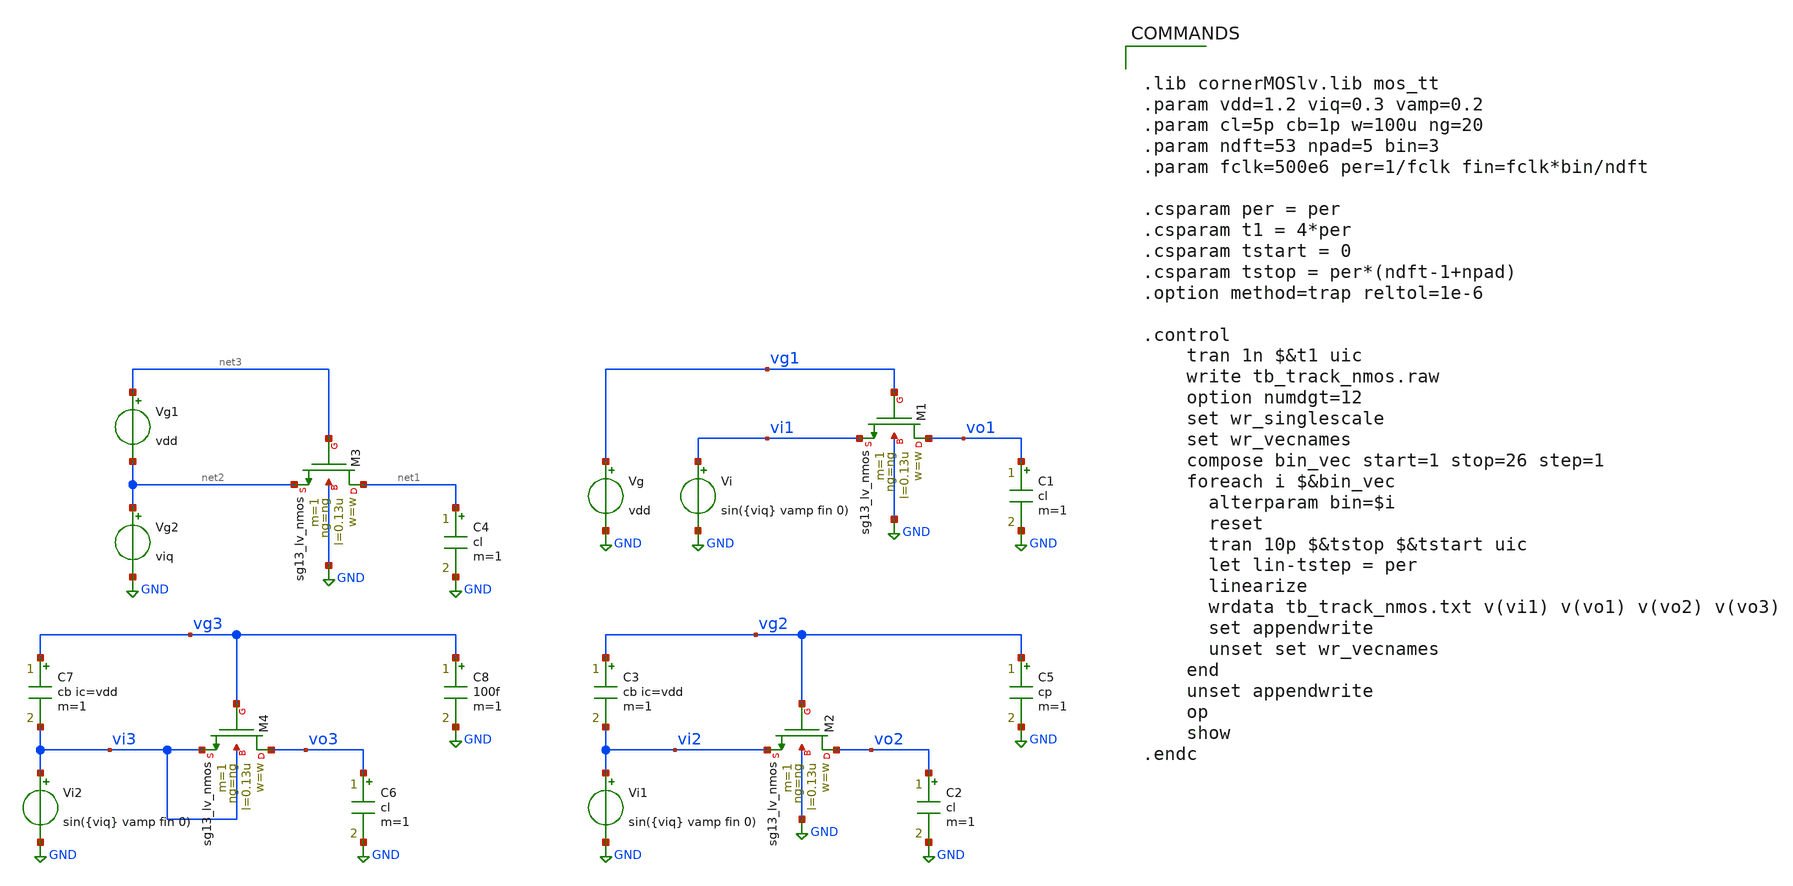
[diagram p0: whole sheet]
** sch_path: xschem/tb_track_nmos.sch
**.subckt tb_track_nmos
Vi vi1 GND sin({viq} vamp fin 0)
Vg vg1 GND vdd
XM1 vo1 vg1 vi1 GND sg13_lv_nmos w=w l=0.13u ng=ng m=1 mm_ok=1
C1 vo1 GND cl m=1
Vi1 vi2 GND sin({viq} vamp fin 0)
XM2 vo2 vg2 vi2 GND sg13_lv_nmos w=w l=0.13u ng=ng m=1 mm_ok=1
C2 vo2 GND cl m=1
C3 vg2 vi2 cb ic=vdd m=1
XM3 net1 net3 net2 GND sg13_lv_nmos w=w l=0.13u ng=ng m=1 mm_ok=1
C4 net1 GND cl m=1
Vg1 net3 net2 vdd
Vg2 net2 GND viq
C5 vg2 GND cp m=1
Vi2 vi3 GND sin({viq} vamp fin 0)
XM4 vo3 vg3 vi3 vi3 sg13_lv_nmos w=w l=0.13u ng=ng m=1 mm_ok=1
C6 vo3 GND cl m=1
C7 vg3 vi3 cb ic=vdd m=1
C8 vg3 GND 100f m=1
**** begin user architecture code


.lib cornerMOSlv.lib mos_tt
.param vdd=1.2 viq=0.3 vamp=0.2
.param cl=5p cb=1p w=100u ng=20
.param ndft=53 npad=5 bin=3
.param fclk=500e6 per=1/fclk fin=fclk*bin/ndft

.csparam per = per
.csparam t1 = 4*per
.csparam tstart = 0
.csparam tstop = per*(ndft-1+npad)
.option method=trap reltol=1e-6

.control
    tran 1n $&t1 uic
    write tb_track_nmos.raw
    option numdgt=12
    set wr_singlescale
    set wr_vecnames
    compose bin_vec start=1 stop=26 step=1
    foreach i $&bin_vec
      alterparam bin=$i
      reset
      tran 10p $&tstop $&tstart uic
      let lin-tstep = per
      linearize
      wrdata tb_track_nmos.txt v(vi1) v(vo1) v(vo2) v(vo3)
      set appendwrite
      unset set wr_vecnames
    end
    unset appendwrite
    op
    show
.endc


**** end user architecture code
**.ends
.GLOBAL GND
.end
